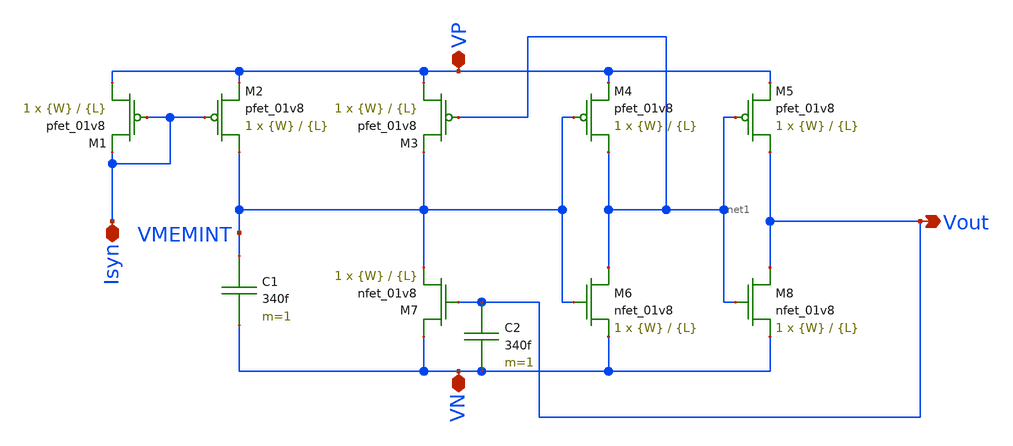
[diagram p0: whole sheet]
** sch_path: schematic/besrour_neuron.sch
**.subckt besrour_neuron Vout VP VN Isyn
*.opin Vout
*.iopin VP
*.iopin VN
*.iopin Isyn
XM1 VP Isyn Isyn VDD sky130_fd_pr__pfet_01v8 L={L} W={W} nf=1 ad='int((nf+1)/2) * W/nf * 0.29' as='int((nf+2)/2) * W/nf * 0.29'
+ pd='2*int((nf+1)/2) * (W/nf + 0.29)' ps='2*int((nf+2)/2) * (W/nf + 0.29)' nrd='0.29 / W' nrs='0.29 / W'
+ sa=0 sb=0 sd=0 mult=1 m=1
XM7 VN Vout VMEMINT GND sky130_fd_pr__nfet_01v8 L={L} W={W} nf=1 ad='int((nf+1)/2) * W/nf * 0.29' as='int((nf+2)/2) * W/nf * 0.29'
+ pd='2*int((nf+1)/2) * (W/nf + 0.29)' ps='2*int((nf+2)/2) * (W/nf + 0.29)' nrd='0.29 / W' nrs='0.29 / W'
+ sa=0 sb=0 sd=0 mult=1 m=1
XM2 VMEMINT Isyn VP VDD sky130_fd_pr__pfet_01v8 L={L} W={W} nf=1 ad='int((nf+1)/2) * W/nf * 0.29' as='int((nf+2)/2) * W/nf * 0.29'
+ pd='2*int((nf+1)/2) * (W/nf + 0.29)' ps='2*int((nf+2)/2) * (W/nf + 0.29)' nrd='0.29 / W' nrs='0.29 / W'
+ sa=0 sb=0 sd=0 mult=1 m=1
XM3 VP net1 VMEMINT VDD sky130_fd_pr__pfet_01v8 L={L} W={W} nf=1 ad='int((nf+1)/2) * W/nf * 0.29' as='int((nf+2)/2) * W/nf * 0.29'
+ pd='2*int((nf+1)/2) * (W/nf + 0.29)' ps='2*int((nf+2)/2) * (W/nf + 0.29)' nrd='0.29 / W' nrs='0.29 / W'
+ sa=0 sb=0 sd=0 mult=1 m=1
XM4 net1 VMEMINT VP VDD sky130_fd_pr__pfet_01v8 L={L} W={W} nf=1 ad='int((nf+1)/2) * W/nf * 0.29' as='int((nf+2)/2) * W/nf * 0.29'
+ pd='2*int((nf+1)/2) * (W/nf + 0.29)' ps='2*int((nf+2)/2) * (W/nf + 0.29)' nrd='0.29 / W' nrs='0.29 / W'
+ sa=0 sb=0 sd=0 mult=1 m=1
XM5 Vout net1 VP VDD sky130_fd_pr__pfet_01v8 L={L} W={W} nf=1 ad='int((nf+1)/2) * W/nf * 0.29' as='int((nf+2)/2) * W/nf * 0.29'
+ pd='2*int((nf+1)/2) * (W/nf + 0.29)' ps='2*int((nf+2)/2) * (W/nf + 0.29)' nrd='0.29 / W' nrs='0.29 / W'
+ sa=0 sb=0 sd=0 mult=1 m=1
XM6 net1 VMEMINT VN GND sky130_fd_pr__nfet_01v8 L={L} W={W} nf=1 ad='int((nf+1)/2) * W/nf * 0.29' as='int((nf+2)/2) * W/nf * 0.29'
+ pd='2*int((nf+1)/2) * (W/nf + 0.29)' ps='2*int((nf+2)/2) * (W/nf + 0.29)' nrd='0.29 / W' nrs='0.29 / W'
+ sa=0 sb=0 sd=0 mult=1 m=1
XM8 Vout net1 VN GND sky130_fd_pr__nfet_01v8 L={L} W={W} nf=1 ad='int((nf+1)/2) * W/nf * 0.29' as='int((nf+2)/2) * W/nf * 0.29'
+ pd='2*int((nf+1)/2) * (W/nf + 0.29)' ps='2*int((nf+2)/2) * (W/nf + 0.29)' nrd='0.29 / W' nrs='0.29 / W'
+ sa=0 sb=0 sd=0 mult=1 m=1
C1 VMEMINT VN 340f m=1
C2 Vout VN 340f m=1
**.ends
.end
